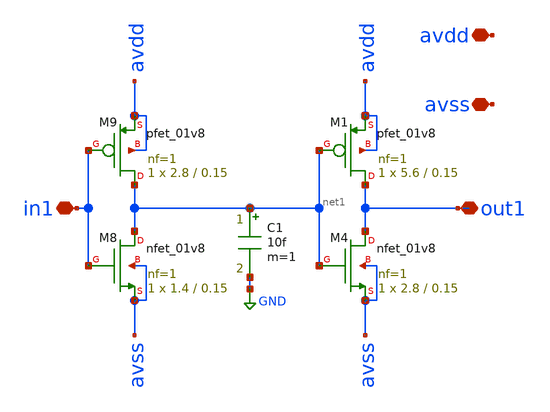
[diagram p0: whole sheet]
** sch_path: xschem/inv_buffer2.sch
**.subckt inv_buffer2 in1 out1 avdd avss
*.iopin in1
*.iopin out1
*.iopin avdd
*.iopin avss
XM8 net1 in1 avss avss sky130_fd_pr__nfet_01v8 L=0.15 W=1.4 nf=1 ad='int((nf+1)/2) * W/nf * 0.29' as='int((nf+2)/2) * W/nf * 0.29'
+ pd='2*int((nf+1)/2) * (W/nf + 0.29)' ps='2*int((nf+2)/2) * (W/nf + 0.29)' nrd='0.29 / W' nrs='0.29 / W'
+ sa=0 sb=0 sd=0 mult=1 m=1
XM9 net1 in1 avdd avdd sky130_fd_pr__pfet_01v8 L=0.15 W=2.8 nf=1 ad='int((nf+1)/2) * W/nf * 0.29' as='int((nf+2)/2) * W/nf * 0.29'
+ pd='2*int((nf+1)/2) * (W/nf + 0.29)' ps='2*int((nf+2)/2) * (W/nf + 0.29)' nrd='0.29 / W' nrs='0.29 / W'
+ sa=0 sb=0 sd=0 mult=1 m=1
XM4 out1 net1 avss avss sky130_fd_pr__nfet_01v8 L=0.15 W=2.8 nf=1 ad='int((nf+1)/2) * W/nf * 0.29' as='int((nf+2)/2) * W/nf * 0.29'
+ pd='2*int((nf+1)/2) * (W/nf + 0.29)' ps='2*int((nf+2)/2) * (W/nf + 0.29)' nrd='0.29 / W' nrs='0.29 / W'
+ sa=0 sb=0 sd=0 mult=1 m=1
C1 net1 GND 10f m=1
XM1 out1 net1 avdd avdd sky130_fd_pr__pfet_01v8 L=0.15 W=5.6 nf=1 ad='int((nf+1)/2) * W/nf * 0.29' as='int((nf+2)/2) * W/nf * 0.29'
+ pd='2*int((nf+1)/2) * (W/nf + 0.29)' ps='2*int((nf+2)/2) * (W/nf + 0.29)' nrd='0.29 / W' nrs='0.29 / W'
+ sa=0 sb=0 sd=0 mult=1 m=1
**.ends
.GLOBAL GND
.end
